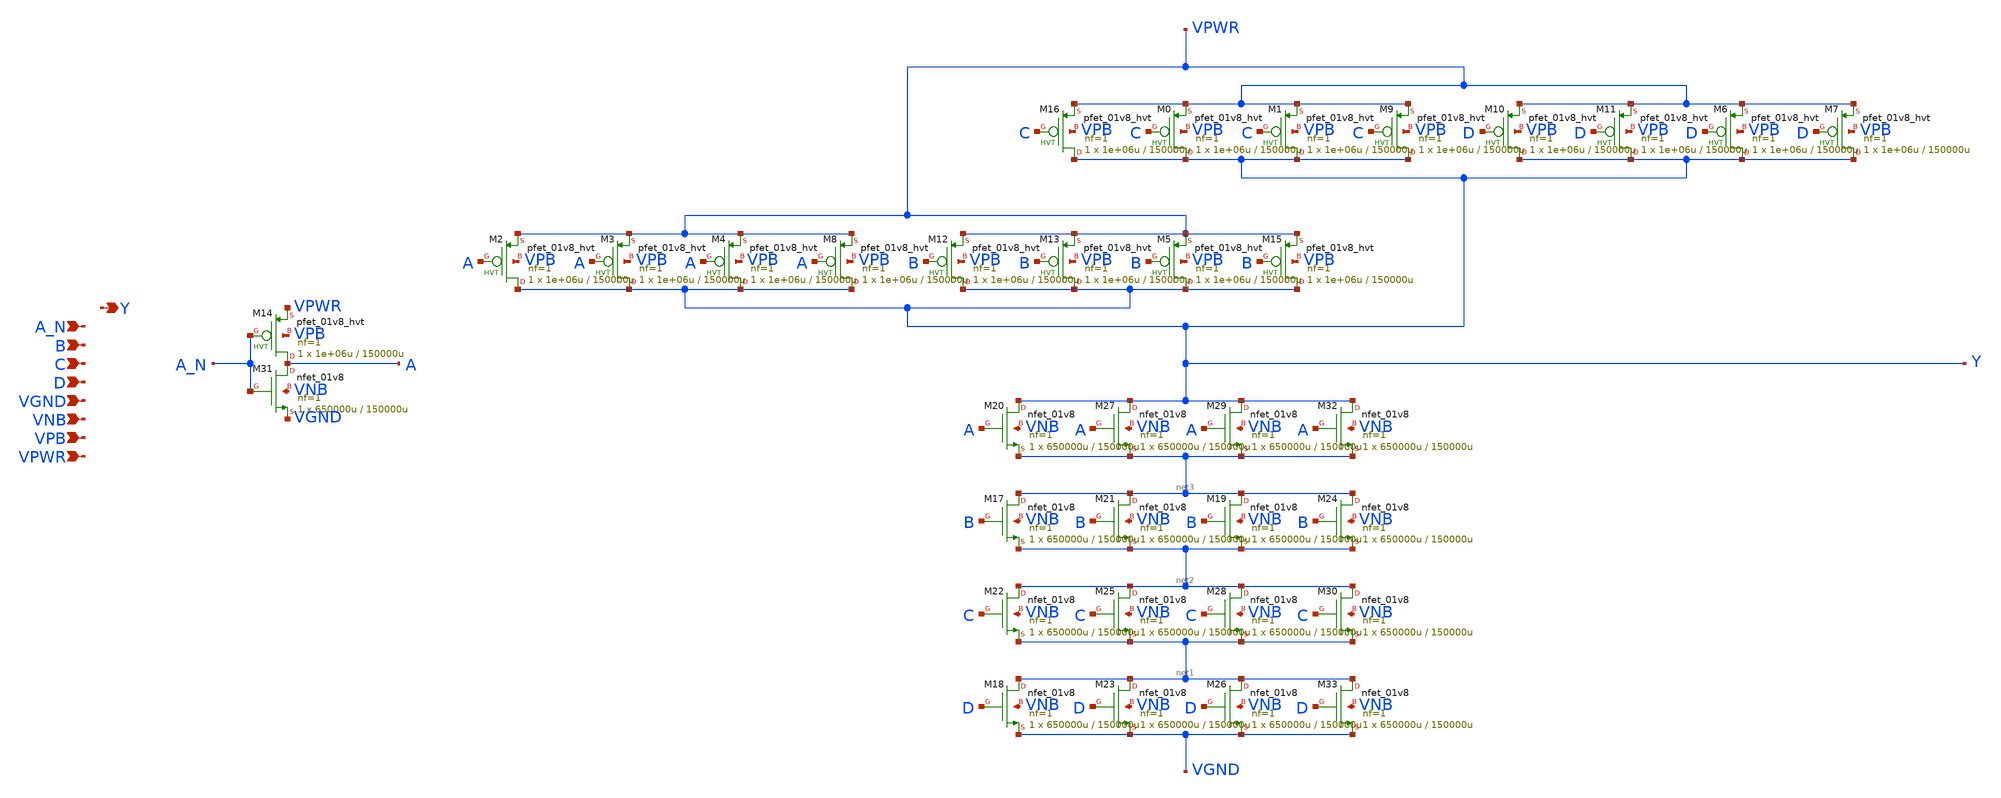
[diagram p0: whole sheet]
** sch_path: schematics/nand4b/sky130_fd_sc_hd__nand4b_4.sch
**.subckt sky130_fd_sc_hd__nand4b_4 A_N B C D VGND VNB VPB VPWR Y
*.ipin A_N
*.ipin B
*.ipin C
*.ipin D
*.ipin VGND
*.ipin VNB
*.ipin VPB
*.ipin VPWR
*.opin Y
XM0 Y C VPWR VPB sky130_fd_pr__pfet_01v8_hvt L=150000u W=1e+06u nf=1 ad='int((1 + 1)/2) * 1e+06u / 1 * 0.29'
+ as='int((1 + 2)/2) * 1e+06u / 1 * 0.29' pd='2*int((1 + 1)/2) * (1e+06u / 1 + 0.29)' ps='2*int((1 + 2)/2) * (1e+06u / 1 + 0.29)'
+ nrd='0.29 / 1e+06u ' nrs='0.29 / 1e+06u ' sa=0 sb=0 sd=0 mult=1 m=1
XM1 Y C VPWR VPB sky130_fd_pr__pfet_01v8_hvt L=150000u W=1e+06u nf=1 ad='int((1 + 1)/2) * 1e+06u / 1 * 0.29'
+ as='int((1 + 2)/2) * 1e+06u / 1 * 0.29' pd='2*int((1 + 1)/2) * (1e+06u / 1 + 0.29)' ps='2*int((1 + 2)/2) * (1e+06u / 1 + 0.29)'
+ nrd='0.29 / 1e+06u ' nrs='0.29 / 1e+06u ' sa=0 sb=0 sd=0 mult=1 m=1
XM2 Y A VPWR VPB sky130_fd_pr__pfet_01v8_hvt L=150000u W=1e+06u nf=1 ad='int((1 + 1)/2) * 1e+06u / 1 * 0.29'
+ as='int((1 + 2)/2) * 1e+06u / 1 * 0.29' pd='2*int((1 + 1)/2) * (1e+06u / 1 + 0.29)' ps='2*int((1 + 2)/2) * (1e+06u / 1 + 0.29)'
+ nrd='0.29 / 1e+06u ' nrs='0.29 / 1e+06u ' sa=0 sb=0 sd=0 mult=1 m=1
XM3 Y A VPWR VPB sky130_fd_pr__pfet_01v8_hvt L=150000u W=1e+06u nf=1 ad='int((1 + 1)/2) * 1e+06u / 1 * 0.29'
+ as='int((1 + 2)/2) * 1e+06u / 1 * 0.29' pd='2*int((1 + 1)/2) * (1e+06u / 1 + 0.29)' ps='2*int((1 + 2)/2) * (1e+06u / 1 + 0.29)'
+ nrd='0.29 / 1e+06u ' nrs='0.29 / 1e+06u ' sa=0 sb=0 sd=0 mult=1 m=1
XM4 Y A VPWR VPB sky130_fd_pr__pfet_01v8_hvt L=150000u W=1e+06u nf=1 ad='int((1 + 1)/2) * 1e+06u / 1 * 0.29'
+ as='int((1 + 2)/2) * 1e+06u / 1 * 0.29' pd='2*int((1 + 1)/2) * (1e+06u / 1 + 0.29)' ps='2*int((1 + 2)/2) * (1e+06u / 1 + 0.29)'
+ nrd='0.29 / 1e+06u ' nrs='0.29 / 1e+06u ' sa=0 sb=0 sd=0 mult=1 m=1
XM5 Y B VPWR VPB sky130_fd_pr__pfet_01v8_hvt L=150000u W=1e+06u nf=1 ad='int((1 + 1)/2) * 1e+06u / 1 * 0.29'
+ as='int((1 + 2)/2) * 1e+06u / 1 * 0.29' pd='2*int((1 + 1)/2) * (1e+06u / 1 + 0.29)' ps='2*int((1 + 2)/2) * (1e+06u / 1 + 0.29)'
+ nrd='0.29 / 1e+06u ' nrs='0.29 / 1e+06u ' sa=0 sb=0 sd=0 mult=1 m=1
XM6 Y D VPWR VPB sky130_fd_pr__pfet_01v8_hvt L=150000u W=1e+06u nf=1 ad='int((1 + 1)/2) * 1e+06u / 1 * 0.29'
+ as='int((1 + 2)/2) * 1e+06u / 1 * 0.29' pd='2*int((1 + 1)/2) * (1e+06u / 1 + 0.29)' ps='2*int((1 + 2)/2) * (1e+06u / 1 + 0.29)'
+ nrd='0.29 / 1e+06u ' nrs='0.29 / 1e+06u ' sa=0 sb=0 sd=0 mult=1 m=1
XM7 Y D VPWR VPB sky130_fd_pr__pfet_01v8_hvt L=150000u W=1e+06u nf=1 ad='int((1 + 1)/2) * 1e+06u / 1 * 0.29'
+ as='int((1 + 2)/2) * 1e+06u / 1 * 0.29' pd='2*int((1 + 1)/2) * (1e+06u / 1 + 0.29)' ps='2*int((1 + 2)/2) * (1e+06u / 1 + 0.29)'
+ nrd='0.29 / 1e+06u ' nrs='0.29 / 1e+06u ' sa=0 sb=0 sd=0 mult=1 m=1
XM8 Y A VPWR VPB sky130_fd_pr__pfet_01v8_hvt L=150000u W=1e+06u nf=1 ad='int((1 + 1)/2) * 1e+06u / 1 * 0.29'
+ as='int((1 + 2)/2) * 1e+06u / 1 * 0.29' pd='2*int((1 + 1)/2) * (1e+06u / 1 + 0.29)' ps='2*int((1 + 2)/2) * (1e+06u / 1 + 0.29)'
+ nrd='0.29 / 1e+06u ' nrs='0.29 / 1e+06u ' sa=0 sb=0 sd=0 mult=1 m=1
XM9 Y C VPWR VPB sky130_fd_pr__pfet_01v8_hvt L=150000u W=1e+06u nf=1 ad='int((1 + 1)/2) * 1e+06u / 1 * 0.29'
+ as='int((1 + 2)/2) * 1e+06u / 1 * 0.29' pd='2*int((1 + 1)/2) * (1e+06u / 1 + 0.29)' ps='2*int((1 + 2)/2) * (1e+06u / 1 + 0.29)'
+ nrd='0.29 / 1e+06u ' nrs='0.29 / 1e+06u ' sa=0 sb=0 sd=0 mult=1 m=1
XM10 Y D VPWR VPB sky130_fd_pr__pfet_01v8_hvt L=150000u W=1e+06u nf=1 ad='int((1 + 1)/2) * 1e+06u / 1 * 0.29'
+ as='int((1 + 2)/2) * 1e+06u / 1 * 0.29' pd='2*int((1 + 1)/2) * (1e+06u / 1 + 0.29)' ps='2*int((1 + 2)/2) * (1e+06u / 1 + 0.29)'
+ nrd='0.29 / 1e+06u ' nrs='0.29 / 1e+06u ' sa=0 sb=0 sd=0 mult=1 m=1
XM11 Y D VPWR VPB sky130_fd_pr__pfet_01v8_hvt L=150000u W=1e+06u nf=1 ad='int((1 + 1)/2) * 1e+06u / 1 * 0.29'
+ as='int((1 + 2)/2) * 1e+06u / 1 * 0.29' pd='2*int((1 + 1)/2) * (1e+06u / 1 + 0.29)' ps='2*int((1 + 2)/2) * (1e+06u / 1 + 0.29)'
+ nrd='0.29 / 1e+06u ' nrs='0.29 / 1e+06u ' sa=0 sb=0 sd=0 mult=1 m=1
XM12 Y B VPWR VPB sky130_fd_pr__pfet_01v8_hvt L=150000u W=1e+06u nf=1 ad='int((1 + 1)/2) * 1e+06u / 1 * 0.29'
+ as='int((1 + 2)/2) * 1e+06u / 1 * 0.29' pd='2*int((1 + 1)/2) * (1e+06u / 1 + 0.29)' ps='2*int((1 + 2)/2) * (1e+06u / 1 + 0.29)'
+ nrd='0.29 / 1e+06u ' nrs='0.29 / 1e+06u ' sa=0 sb=0 sd=0 mult=1 m=1
XM13 Y B VPWR VPB sky130_fd_pr__pfet_01v8_hvt L=150000u W=1e+06u nf=1 ad='int((1 + 1)/2) * 1e+06u / 1 * 0.29'
+ as='int((1 + 2)/2) * 1e+06u / 1 * 0.29' pd='2*int((1 + 1)/2) * (1e+06u / 1 + 0.29)' ps='2*int((1 + 2)/2) * (1e+06u / 1 + 0.29)'
+ nrd='0.29 / 1e+06u ' nrs='0.29 / 1e+06u ' sa=0 sb=0 sd=0 mult=1 m=1
XM14 A A_N VPWR VPB sky130_fd_pr__pfet_01v8_hvt L=150000u W=1e+06u nf=1 ad='int((1 + 1)/2) * 1e+06u / 1 * 0.29'
+ as='int((1 + 2)/2) * 1e+06u / 1 * 0.29' pd='2*int((1 + 1)/2) * (1e+06u / 1 + 0.29)' ps='2*int((1 + 2)/2) * (1e+06u / 1 + 0.29)'
+ nrd='0.29 / 1e+06u ' nrs='0.29 / 1e+06u ' sa=0 sb=0 sd=0 mult=1 m=1
XM15 Y B VPWR VPB sky130_fd_pr__pfet_01v8_hvt L=150000u W=1e+06u nf=1 ad='int((1 + 1)/2) * 1e+06u / 1 * 0.29'
+ as='int((1 + 2)/2) * 1e+06u / 1 * 0.29' pd='2*int((1 + 1)/2) * (1e+06u / 1 + 0.29)' ps='2*int((1 + 2)/2) * (1e+06u / 1 + 0.29)'
+ nrd='0.29 / 1e+06u ' nrs='0.29 / 1e+06u ' sa=0 sb=0 sd=0 mult=1 m=1
XM16 Y C VPWR VPB sky130_fd_pr__pfet_01v8_hvt L=150000u W=1e+06u nf=1 ad='int((1 + 1)/2) * 1e+06u / 1 * 0.29'
+ as='int((1 + 2)/2) * 1e+06u / 1 * 0.29' pd='2*int((1 + 1)/2) * (1e+06u / 1 + 0.29)' ps='2*int((1 + 2)/2) * (1e+06u / 1 + 0.29)'
+ nrd='0.29 / 1e+06u ' nrs='0.29 / 1e+06u ' sa=0 sb=0 sd=0 mult=1 m=1
XM17 net3 B net2 VNB sky130_fd_pr__nfet_01v8 L=150000u W=650000u nf=1 ad='int((1 + 1)/2) * 650000u / 1 * 0.29'
+ as='int((1 + 2)/2) * 650000u / 1 * 0.29' pd='2*int((1 + 1)/2) * (650000u / 1 + 0.29)' ps='2*int((1 + 2)/2) * (650000u / 1 + 0.29)'
+ nrd='0.29 / 650000u ' nrs='0.29 / 650000u ' sa=0 sb=0 sd=0 mult=1 m=1
XM18 net1 D VGND VNB sky130_fd_pr__nfet_01v8 L=150000u W=650000u nf=1 ad='int((1 + 1)/2) * 650000u / 1 * 0.29'
+ as='int((1 + 2)/2) * 650000u / 1 * 0.29' pd='2*int((1 + 1)/2) * (650000u / 1 + 0.29)' ps='2*int((1 + 2)/2) * (650000u / 1 + 0.29)'
+ nrd='0.29 / 650000u ' nrs='0.29 / 650000u ' sa=0 sb=0 sd=0 mult=1 m=1
XM19 net3 B net2 VNB sky130_fd_pr__nfet_01v8 L=150000u W=650000u nf=1 ad='int((1 + 1)/2) * 650000u / 1 * 0.29'
+ as='int((1 + 2)/2) * 650000u / 1 * 0.29' pd='2*int((1 + 1)/2) * (650000u / 1 + 0.29)' ps='2*int((1 + 2)/2) * (650000u / 1 + 0.29)'
+ nrd='0.29 / 650000u ' nrs='0.29 / 650000u ' sa=0 sb=0 sd=0 mult=1 m=1
XM20 Y A net3 VNB sky130_fd_pr__nfet_01v8 L=150000u W=650000u nf=1 ad='int((1 + 1)/2) * 650000u / 1 * 0.29'
+ as='int((1 + 2)/2) * 650000u / 1 * 0.29' pd='2*int((1 + 1)/2) * (650000u / 1 + 0.29)' ps='2*int((1 + 2)/2) * (650000u / 1 + 0.29)'
+ nrd='0.29 / 650000u ' nrs='0.29 / 650000u ' sa=0 sb=0 sd=0 mult=1 m=1
XM21 net3 B net2 VNB sky130_fd_pr__nfet_01v8 L=150000u W=650000u nf=1 ad='int((1 + 1)/2) * 650000u / 1 * 0.29'
+ as='int((1 + 2)/2) * 650000u / 1 * 0.29' pd='2*int((1 + 1)/2) * (650000u / 1 + 0.29)' ps='2*int((1 + 2)/2) * (650000u / 1 + 0.29)'
+ nrd='0.29 / 650000u ' nrs='0.29 / 650000u ' sa=0 sb=0 sd=0 mult=1 m=1
XM22 net2 C net1 VNB sky130_fd_pr__nfet_01v8 L=150000u W=650000u nf=1 ad='int((1 + 1)/2) * 650000u / 1 * 0.29'
+ as='int((1 + 2)/2) * 650000u / 1 * 0.29' pd='2*int((1 + 1)/2) * (650000u / 1 + 0.29)' ps='2*int((1 + 2)/2) * (650000u / 1 + 0.29)'
+ nrd='0.29 / 650000u ' nrs='0.29 / 650000u ' sa=0 sb=0 sd=0 mult=1 m=1
XM23 net1 D VGND VNB sky130_fd_pr__nfet_01v8 L=150000u W=650000u nf=1 ad='int((1 + 1)/2) * 650000u / 1 * 0.29'
+ as='int((1 + 2)/2) * 650000u / 1 * 0.29' pd='2*int((1 + 1)/2) * (650000u / 1 + 0.29)' ps='2*int((1 + 2)/2) * (650000u / 1 + 0.29)'
+ nrd='0.29 / 650000u ' nrs='0.29 / 650000u ' sa=0 sb=0 sd=0 mult=1 m=1
XM24 net3 B net2 VNB sky130_fd_pr__nfet_01v8 L=150000u W=650000u nf=1 ad='int((1 + 1)/2) * 650000u / 1 * 0.29'
+ as='int((1 + 2)/2) * 650000u / 1 * 0.29' pd='2*int((1 + 1)/2) * (650000u / 1 + 0.29)' ps='2*int((1 + 2)/2) * (650000u / 1 + 0.29)'
+ nrd='0.29 / 650000u ' nrs='0.29 / 650000u ' sa=0 sb=0 sd=0 mult=1 m=1
XM25 net2 C net1 VNB sky130_fd_pr__nfet_01v8 L=150000u W=650000u nf=1 ad='int((1 + 1)/2) * 650000u / 1 * 0.29'
+ as='int((1 + 2)/2) * 650000u / 1 * 0.29' pd='2*int((1 + 1)/2) * (650000u / 1 + 0.29)' ps='2*int((1 + 2)/2) * (650000u / 1 + 0.29)'
+ nrd='0.29 / 650000u ' nrs='0.29 / 650000u ' sa=0 sb=0 sd=0 mult=1 m=1
XM26 net1 D VGND VNB sky130_fd_pr__nfet_01v8 L=150000u W=650000u nf=1 ad='int((1 + 1)/2) * 650000u / 1 * 0.29'
+ as='int((1 + 2)/2) * 650000u / 1 * 0.29' pd='2*int((1 + 1)/2) * (650000u / 1 + 0.29)' ps='2*int((1 + 2)/2) * (650000u / 1 + 0.29)'
+ nrd='0.29 / 650000u ' nrs='0.29 / 650000u ' sa=0 sb=0 sd=0 mult=1 m=1
XM27 Y A net3 VNB sky130_fd_pr__nfet_01v8 L=150000u W=650000u nf=1 ad='int((1 + 1)/2) * 650000u / 1 * 0.29'
+ as='int((1 + 2)/2) * 650000u / 1 * 0.29' pd='2*int((1 + 1)/2) * (650000u / 1 + 0.29)' ps='2*int((1 + 2)/2) * (650000u / 1 + 0.29)'
+ nrd='0.29 / 650000u ' nrs='0.29 / 650000u ' sa=0 sb=0 sd=0 mult=1 m=1
XM28 net2 C net1 VNB sky130_fd_pr__nfet_01v8 L=150000u W=650000u nf=1 ad='int((1 + 1)/2) * 650000u / 1 * 0.29'
+ as='int((1 + 2)/2) * 650000u / 1 * 0.29' pd='2*int((1 + 1)/2) * (650000u / 1 + 0.29)' ps='2*int((1 + 2)/2) * (650000u / 1 + 0.29)'
+ nrd='0.29 / 650000u ' nrs='0.29 / 650000u ' sa=0 sb=0 sd=0 mult=1 m=1
XM29 Y A net3 VNB sky130_fd_pr__nfet_01v8 L=150000u W=650000u nf=1 ad='int((1 + 1)/2) * 650000u / 1 * 0.29'
+ as='int((1 + 2)/2) * 650000u / 1 * 0.29' pd='2*int((1 + 1)/2) * (650000u / 1 + 0.29)' ps='2*int((1 + 2)/2) * (650000u / 1 + 0.29)'
+ nrd='0.29 / 650000u ' nrs='0.29 / 650000u ' sa=0 sb=0 sd=0 mult=1 m=1
XM30 net2 C net1 VNB sky130_fd_pr__nfet_01v8 L=150000u W=650000u nf=1 ad='int((1 + 1)/2) * 650000u / 1 * 0.29'
+ as='int((1 + 2)/2) * 650000u / 1 * 0.29' pd='2*int((1 + 1)/2) * (650000u / 1 + 0.29)' ps='2*int((1 + 2)/2) * (650000u / 1 + 0.29)'
+ nrd='0.29 / 650000u ' nrs='0.29 / 650000u ' sa=0 sb=0 sd=0 mult=1 m=1
XM32 Y A net3 VNB sky130_fd_pr__nfet_01v8 L=150000u W=650000u nf=1 ad='int((1 + 1)/2) * 650000u / 1 * 0.29'
+ as='int((1 + 2)/2) * 650000u / 1 * 0.29' pd='2*int((1 + 1)/2) * (650000u / 1 + 0.29)' ps='2*int((1 + 2)/2) * (650000u / 1 + 0.29)'
+ nrd='0.29 / 650000u ' nrs='0.29 / 650000u ' sa=0 sb=0 sd=0 mult=1 m=1
XM33 net1 D VGND VNB sky130_fd_pr__nfet_01v8 L=150000u W=650000u nf=1 ad='int((1 + 1)/2) * 650000u / 1 * 0.29'
+ as='int((1 + 2)/2) * 650000u / 1 * 0.29' pd='2*int((1 + 1)/2) * (650000u / 1 + 0.29)' ps='2*int((1 + 2)/2) * (650000u / 1 + 0.29)'
+ nrd='0.29 / 650000u ' nrs='0.29 / 650000u ' sa=0 sb=0 sd=0 mult=1 m=1
XM31 A A_N VGND VNB sky130_fd_pr__nfet_01v8 L=150000u W=650000u nf=1 ad='int((1 + 1)/2) * 650000u / 1 * 0.29'
+ as='int((1 + 2)/2) * 650000u / 1 * 0.29' pd='2*int((1 + 1)/2) * (650000u / 1 + 0.29)' ps='2*int((1 + 2)/2) * (650000u / 1 + 0.29)'
+ nrd='0.29 / 650000u ' nrs='0.29 / 650000u ' sa=0 sb=0 sd=0 mult=1 m=1
**.ends
.end
